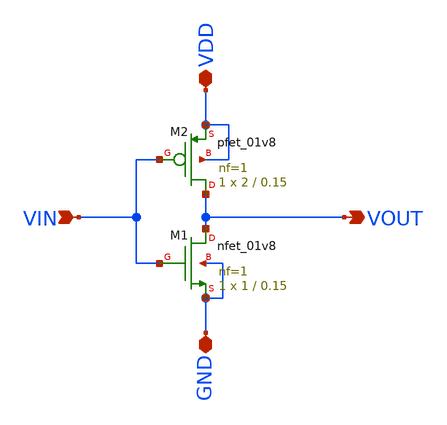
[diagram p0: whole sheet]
** sch_path: Circuits/Examples/Digital/NOT/Inverter_xschem.sch
**.subckt Inverter_xschem VOUT VIN VDD GND
*.opin VOUT
*.ipin VIN
*.iopin VDD
*.iopin GND
XM1 VOUT VIN GND GND sky130_fd_pr__nfet_01v8 L=0.15 W=1 nf=1 ad='int((nf+1)/2) * W/nf * 0.29' as='int((nf+2)/2) * W/nf * 0.29'
+ pd='2*int((nf+1)/2) * (W/nf + 0.29)' ps='2*int((nf+2)/2) * (W/nf + 0.29)' nrd='0.29 / W' nrs='0.29 / W'
+ sa=0 sb=0 sd=0 mult=1 m=1
XM2 VOUT VIN VDD VDD sky130_fd_pr__pfet_01v8 L=0.15 W=2 nf=1 ad='int((nf+1)/2) * W/nf * 0.29' as='int((nf+2)/2) * W/nf * 0.29'
+ pd='2*int((nf+1)/2) * (W/nf + 0.29)' ps='2*int((nf+2)/2) * (W/nf + 0.29)' nrd='0.29 / W' nrs='0.29 / W'
+ sa=0 sb=0 sd=0 mult=1 m=1
**.ends
.end
